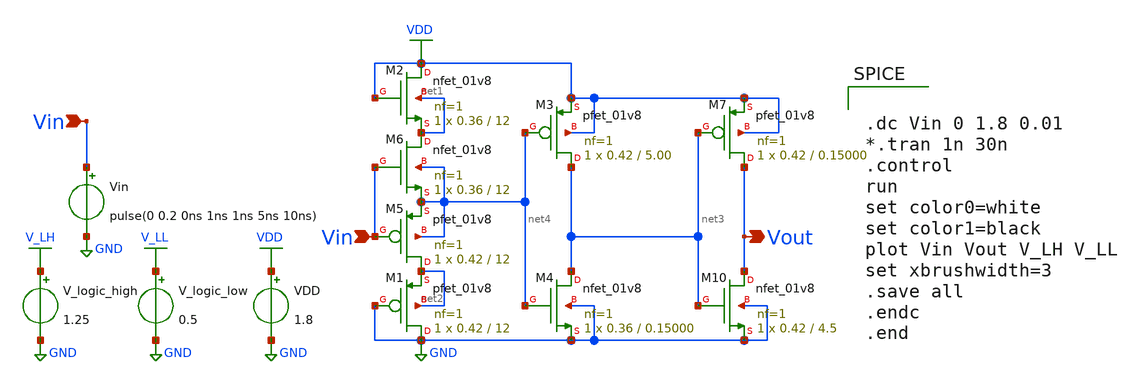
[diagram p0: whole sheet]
** sch_path: xschem/Vth_sch/op-amp.sch
**.subckt op-amp Vin Vin Vout
*.ipin Vin
*.ipin Vin
*.opin Vout
VDD VDD GND 1.8
Vin Vin GND pulse(0 0.2 0ns 1ns 1ns 5ns 10ns)
V_logic_high V_LH GND 1.25
V_logic_low V_LL GND 0.5
XM1 GND GND net2 net2 sky130_fd_pr__pfet_01v8 L=12 W=0.42 nf=1 ad='int((nf+1)/2) * W/nf * 0.29' as='int((nf+2)/2) * W/nf * 0.29'
+ pd='2*int((nf+1)/2) * (W/nf + 0.29)' ps='2*int((nf+2)/2) * (W/nf + 0.29)' nrd='0.29 / W' nrs='0.29 / W'
+ sa=0 sb=0 sd=0 mult=1 m=1
XM2 VDD VDD net1 net1 sky130_fd_pr__nfet_01v8 L=12 W=0.36 nf=1 ad='int((nf+1)/2) * W/nf * 0.29' as='int((nf+2)/2) * W/nf * 0.29'
+ pd='2*int((nf+1)/2) * (W/nf + 0.29)' ps='2*int((nf+2)/2) * (W/nf + 0.29)' nrd='0.29 / W' nrs='0.29 / W'
+ sa=0 sb=0 sd=0 mult=1 m=1
XM7 Vout net3 VDD VDD sky130_fd_pr__pfet_01v8 L=0.15000 W=0.42 nf=1 ad='int((nf+1)/2) * W/nf * 0.29'
+ as='int((nf+2)/2) * W/nf * 0.29' pd='2*int((nf+1)/2) * (W/nf + 0.29)' ps='2*int((nf+2)/2) * (W/nf + 0.29)'
+ nrd='0.29 / W' nrs='0.29 / W' sa=0 sb=0 sd=0 mult=1 m=1
XM10 Vout net3 GND GND sky130_fd_pr__nfet_01v8 L=4.5 W=0.42 nf=1 ad='int((nf+1)/2) * W/nf * 0.29' as='int((nf+2)/2) * W/nf * 0.29'
+ pd='2*int((nf+1)/2) * (W/nf + 0.29)' ps='2*int((nf+2)/2) * (W/nf + 0.29)' nrd='0.29 / W' nrs='0.29 / W'
+ sa=0 sb=0 sd=0 mult=1 m=1
XM3 net3 net4 VDD VDD sky130_fd_pr__pfet_01v8 L=5.00 W=0.42 nf=1 ad='int((nf+1)/2) * W/nf * 0.29' as='int((nf+2)/2) * W/nf * 0.29'
+ pd='2*int((nf+1)/2) * (W/nf + 0.29)' ps='2*int((nf+2)/2) * (W/nf + 0.29)' nrd='0.29 / W' nrs='0.29 / W'
+ sa=0 sb=0 sd=0 mult=1 m=1
XM4 net3 net4 GND GND sky130_fd_pr__nfet_01v8 L=0.15000 W=0.36 nf=1 ad='int((nf+1)/2) * W/nf * 0.29'
+ as='int((nf+2)/2) * W/nf * 0.29' pd='2*int((nf+1)/2) * (W/nf + 0.29)' ps='2*int((nf+2)/2) * (W/nf + 0.29)'
+ nrd='0.29 / W' nrs='0.29 / W' sa=0 sb=0 sd=0 mult=1 m=1
XM5 net2 Vin net4 net4 sky130_fd_pr__pfet_01v8 L=12 W=0.42 nf=1 ad='int((nf+1)/2) * W/nf * 0.29' as='int((nf+2)/2) * W/nf * 0.29'
+ pd='2*int((nf+1)/2) * (W/nf + 0.29)' ps='2*int((nf+2)/2) * (W/nf + 0.29)' nrd='0.29 / W' nrs='0.29 / W'
+ sa=0 sb=0 sd=0 mult=1 m=1
XM6 net1 Vin net4 net4 sky130_fd_pr__nfet_01v8 L=12 W=0.36 nf=1 ad='int((nf+1)/2) * W/nf * 0.29' as='int((nf+2)/2) * W/nf * 0.29'
+ pd='2*int((nf+1)/2) * (W/nf + 0.29)' ps='2*int((nf+2)/2) * (W/nf + 0.29)' nrd='0.29 / W' nrs='0.29 / W'
+ sa=0 sb=0 sd=0 mult=1 m=1
**** begin user architecture code


.lib /usr/local/share/pdk/sky130A/libs.tech/ngspice/sky130.lib.spice tt

.save all





.dc Vin 0 1.8 0.01
*.tran 1n 30n
.control
run
set color0=white
set color1=black
plot Vin Vout V_LH V_LL
set xbrushwidth=3
.save all
.endc
.end


**** end user architecture code
**.ends
.GLOBAL VDD
.GLOBAL GND
.GLOBAL V_LH
.GLOBAL V_LL
.end
